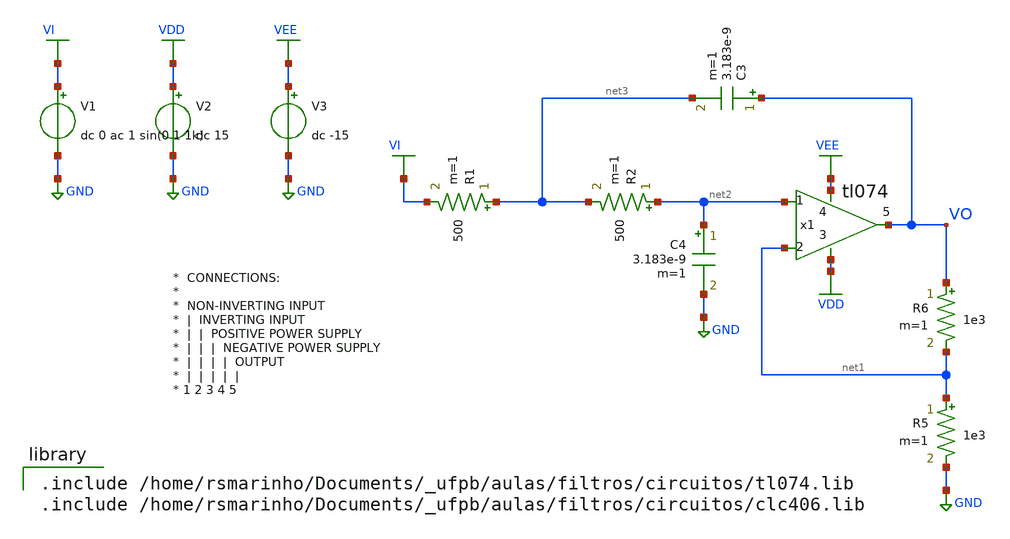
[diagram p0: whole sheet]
** sch_path: circuitos/exemplo11.sch
**.subckt exemplo11
V1 VI GND dc 0 ac 1 sin(0 1 1k)
R6 VO net1 1e3 m=1
R5 net1 GND 1e3 m=1
V2 VDD GND dc 15
V3 VEE GND dc -15
R1 net3 VI 500 m=1
C4 net2 GND 3.183e-9 m=1
x1 net2 net1 VDD VEE VO tl074
R2 net2 net3 500 m=1
C3 VO net3 3.183e-9 m=1
**** begin user architecture code

.include /home/rsmarinho/Documents/_ufpb/aulas/filtros/circuitos/tl074.lib
.include /home/rsmarinho/Documents/_ufpb/aulas/filtros/circuitos/clc406.lib


.control

ac dec 1e2 1e2 1e9
plot xlog db(v(vo)/v(vi))

tran 1e-6 2e-3
plot vi vo

alter @v1[sin] [ 0 1 170000 ]
tran 1e-6 2e-3
plot vi vo

.endc
.end

**** end user architecture code
**.ends
.GLOBAL GND
.GLOBAL VDD
.GLOBAL VI
.GLOBAL VEE
.end
